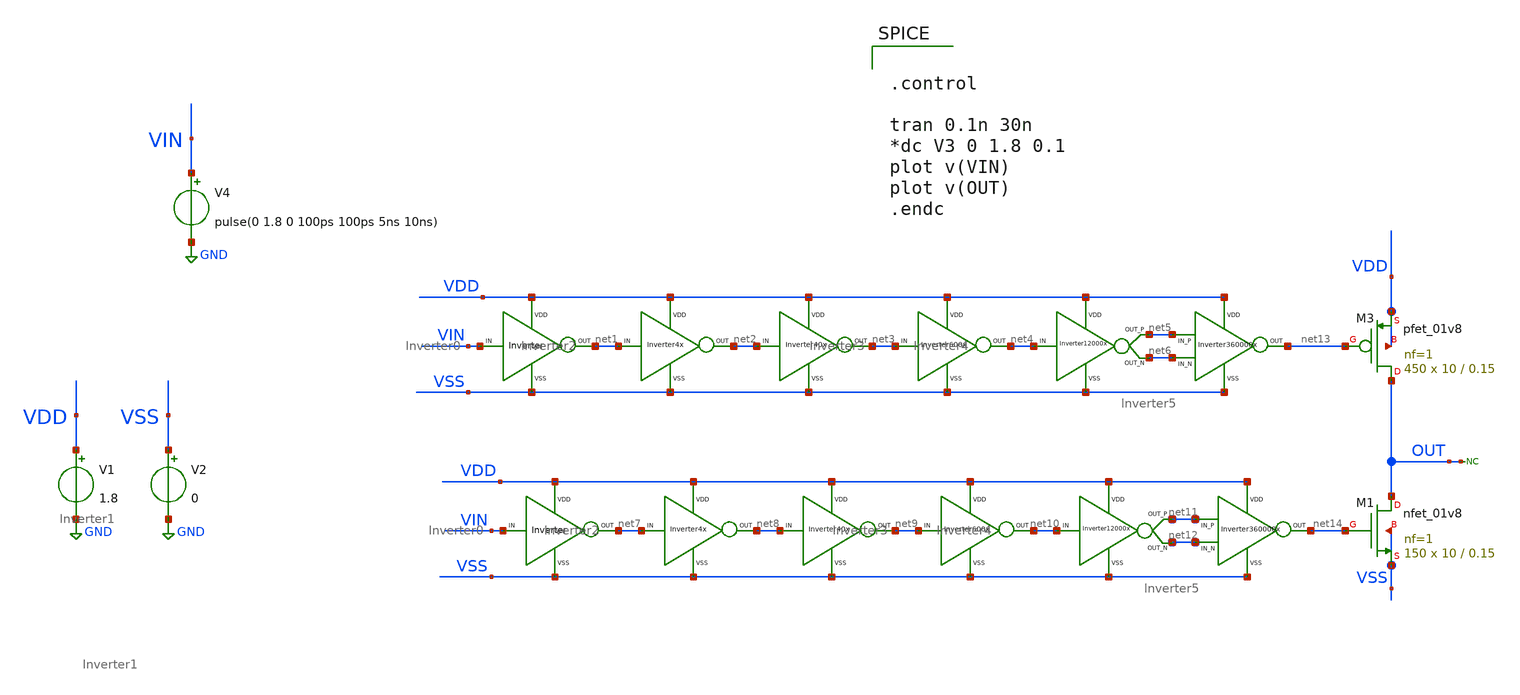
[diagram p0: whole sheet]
** sch_path: xschem/DC_DC_Converter_xschem/OTHERS/DC_DC_Converter_JV9/BUFFER/top.sch
**.subckt top
X1 VIN net1 VDD VSS Inverter0
X2 net1 net2 VDD VSS Inverter1
X3 net2 net3 VDD VSS Inverter2
X4 net3 net4 VDD VSS Inverter3
X5 net4 net5 VDD VSS net6 Inverter4
X6 net13 VDD VSS net5 net6 Inverter5
X7 VIN net7 VDD VSS Inverter0
X8 net7 net8 VDD VSS Inverter1
X9 net8 net9 VDD VSS Inverter2
X10 net9 net10 VDD VSS Inverter3
X11 net10 net11 VDD VSS net12 Inverter4
X12 net14 VDD VSS net11 net12 Inverter5
XM3 OUT net13 VDD VDD sky130_fd_pr__pfet_01v8 L=0.15 W=10 nf=1 ad='int((nf+1)/2) * W/nf * 0.29' as='int((nf+2)/2) * W/nf * 0.29'
+ pd='2*int((nf+1)/2) * (W/nf + 0.29)' ps='2*int((nf+2)/2) * (W/nf + 0.29)' nrd='0.29 / W' nrs='0.29 / W'
+ sa=0 sb=0 sd=0 mult=450 m=450
XM1 OUT net14 VSS VSS sky130_fd_pr__nfet_01v8 L=0.15 W=10 nf=1 ad='int((nf+1)/2) * W/nf * 0.29' as='int((nf+2)/2) * W/nf * 0.29'
+ pd='2*int((nf+1)/2) * (W/nf + 0.29)' ps='2*int((nf+2)/2) * (W/nf + 0.29)' nrd='0.29 / W' nrs='0.29 / W'
+ sa=0 sb=0 sd=0 mult=150 m=150
V1 VDD GND 1.8
V2 VSS GND 0
* noconn OUT
V4 VIN GND pulse(0 1.8 0 100ps 100ps 5ns 10ns)
**** begin user architecture code

** opencircuitdesign pdks install
.lib $::SKYWATER_MODELS/sky130.lib.spice tt




.control

tran 0.1n 30n
*dc V3 0 1.8 0.1
plot v(VIN)
plot v(OUT)
.endc


**** end user architecture code
**.ends
.GLOBAL GND
.end
